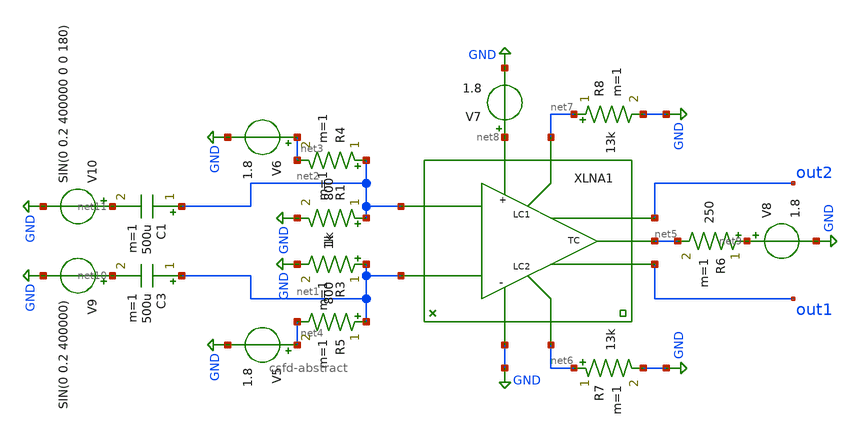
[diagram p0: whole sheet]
** sch_path: xschem/misc/testbank.sch
**.subckt testbank
R1 net2 GND 1k m=1
R3 net1 GND 1k m=1
R4 net2 net3 800 m=1
R5 net1 net4 800 m=1
V5 net4 GND 1.8
V6 net3 GND 1.8
V7 net8 GND 1.8
R6 net9 net5 250 m=1
V8 net9 GND 1.8
R7 net6 GND 13k m=1
R8 net7 GND 13k m=1
V9 net10 GND SIN(0 0.2 400000)
V10 net11 GND SIN(0 0.2 400000 0 0 180)
XLNA1 net2 net1 net8 GND out2 out1 net7 net5 net6 csfd-abstract
C1 net2 net11 500u m=1
C3 net1 net10 500u m=1
**** begin user architecture code
 ** manual skywater pdks install (with patches applied)
* .lib $::SKYWATER_MODELS/models/sky130.lib.spice tt

** opencircuitdesign pdks install
.lib $::SKYWATER_MODELS/sky130.lib.spice tt

.param mc_mm_switch=0
.param mc_pr_switch=0



.tran 0.0000001s 0.000001s
.plot v(drain1) v(drain2)


**** end user architecture code
**.ends

* expanding   symbol:  csfd-abstract.sym # of pins=9
** sym_path: xschem/lownoiseamplifier/csfd-abstract.sym
** sch_path: xschem/lownoiseamplifier/csfd-abstract.sch
.subckt csfd-abstract in1 in2 vdd gnd out1 out2 lc1 tc lc2
*.ipin vdd
*.ipin in1
*.ipin in2
*.ipin gnd
*.opin out1
*.opin out2
*.ipin tc
*.ipin lc1
*.ipin lc2
XM10 out1 in1 net1 gnd sky130_fd_pr__nfet_01v8 L=0.15 W=1 nf=1 ad='int((nf+1)/2) * W/nf * 0.29' as='int((nf+2)/2) * W/nf * 0.29'
+ pd='2*int((nf+1)/2) * (W/nf + 0.29)' ps='2*int((nf+2)/2) * (W/nf + 0.29)' nrd='0.29 / W' nrs='0.29 / W'
+ sa=0 sb=0 sd=0 mult=1 m=1
XM3 out2 lc2 vdd vdd sky130_fd_pr__pfet_01v8 L=0.15 W=1 nf=1 ad='int((nf+1)/2) * W/nf * 0.29' as='int((nf+2)/2) * W/nf * 0.29'
+ pd='2*int((nf+1)/2) * (W/nf + 0.29)' ps='2*int((nf+2)/2) * (W/nf + 0.29)' nrd='0.29 / W' nrs='0.29 / W'
+ sa=0 sb=0 sd=0 mult=1 m=1
XM2 lc2 lc2 vdd vdd sky130_fd_pr__pfet_01v8 L=0.15 W=1 nf=1 ad='int((nf+1)/2) * W/nf * 0.29' as='int((nf+2)/2) * W/nf * 0.29'
+ pd='2*int((nf+1)/2) * (W/nf + 0.29)' ps='2*int((nf+2)/2) * (W/nf + 0.29)' nrd='0.29 / W' nrs='0.29 / W'
+ sa=0 sb=0 sd=0 mult=1 m=1
XM6 lc1 lc1 vdd vdd sky130_fd_pr__pfet_01v8 L=0.15 W=1 nf=1 ad='int((nf+1)/2) * W/nf * 0.29' as='int((nf+2)/2) * W/nf * 0.29'
+ pd='2*int((nf+1)/2) * (W/nf + 0.29)' ps='2*int((nf+2)/2) * (W/nf + 0.29)' nrd='0.29 / W' nrs='0.29 / W'
+ sa=0 sb=0 sd=0 mult=1 m=1
XM7 out1 lc1 vdd vdd sky130_fd_pr__pfet_01v8 L=0.15 W=1 nf=1 ad='int((nf+1)/2) * W/nf * 0.29' as='int((nf+2)/2) * W/nf * 0.29'
+ pd='2*int((nf+1)/2) * (W/nf + 0.29)' ps='2*int((nf+2)/2) * (W/nf + 0.29)' nrd='0.29 / W' nrs='0.29 / W'
+ sa=0 sb=0 sd=0 mult=1 m=1
XM5 out2 in2 net1 gnd sky130_fd_pr__nfet_01v8 L=0.15 W=1 nf=1 ad='int((nf+1)/2) * W/nf * 0.29' as='int((nf+2)/2) * W/nf * 0.29'
+ pd='2*int((nf+1)/2) * (W/nf + 0.29)' ps='2*int((nf+2)/2) * (W/nf + 0.29)' nrd='0.29 / W' nrs='0.29 / W'
+ sa=0 sb=0 sd=0 mult=1 m=1
XM1 net1 tc gnd gnd sky130_fd_pr__nfet_01v8 L=0.15 W=1 nf=1 ad='int((nf+1)/2) * W/nf * 0.29' as='int((nf+2)/2) * W/nf * 0.29'
+ pd='2*int((nf+1)/2) * (W/nf + 0.29)' ps='2*int((nf+2)/2) * (W/nf + 0.29)' nrd='0.29 / W' nrs='0.29 / W'
+ sa=0 sb=0 sd=0 mult=1 m=1
XM4 tc tc gnd gnd sky130_fd_pr__nfet_01v8 L=0.15 W=1 nf=1 ad='int((nf+1)/2) * W/nf * 0.29' as='int((nf+2)/2) * W/nf * 0.29'
+ pd='2*int((nf+1)/2) * (W/nf + 0.29)' ps='2*int((nf+2)/2) * (W/nf + 0.29)' nrd='0.29 / W' nrs='0.29 / W'
+ sa=0 sb=0 sd=0 mult=1 m=1
.ends

.GLOBAL GND
.end
